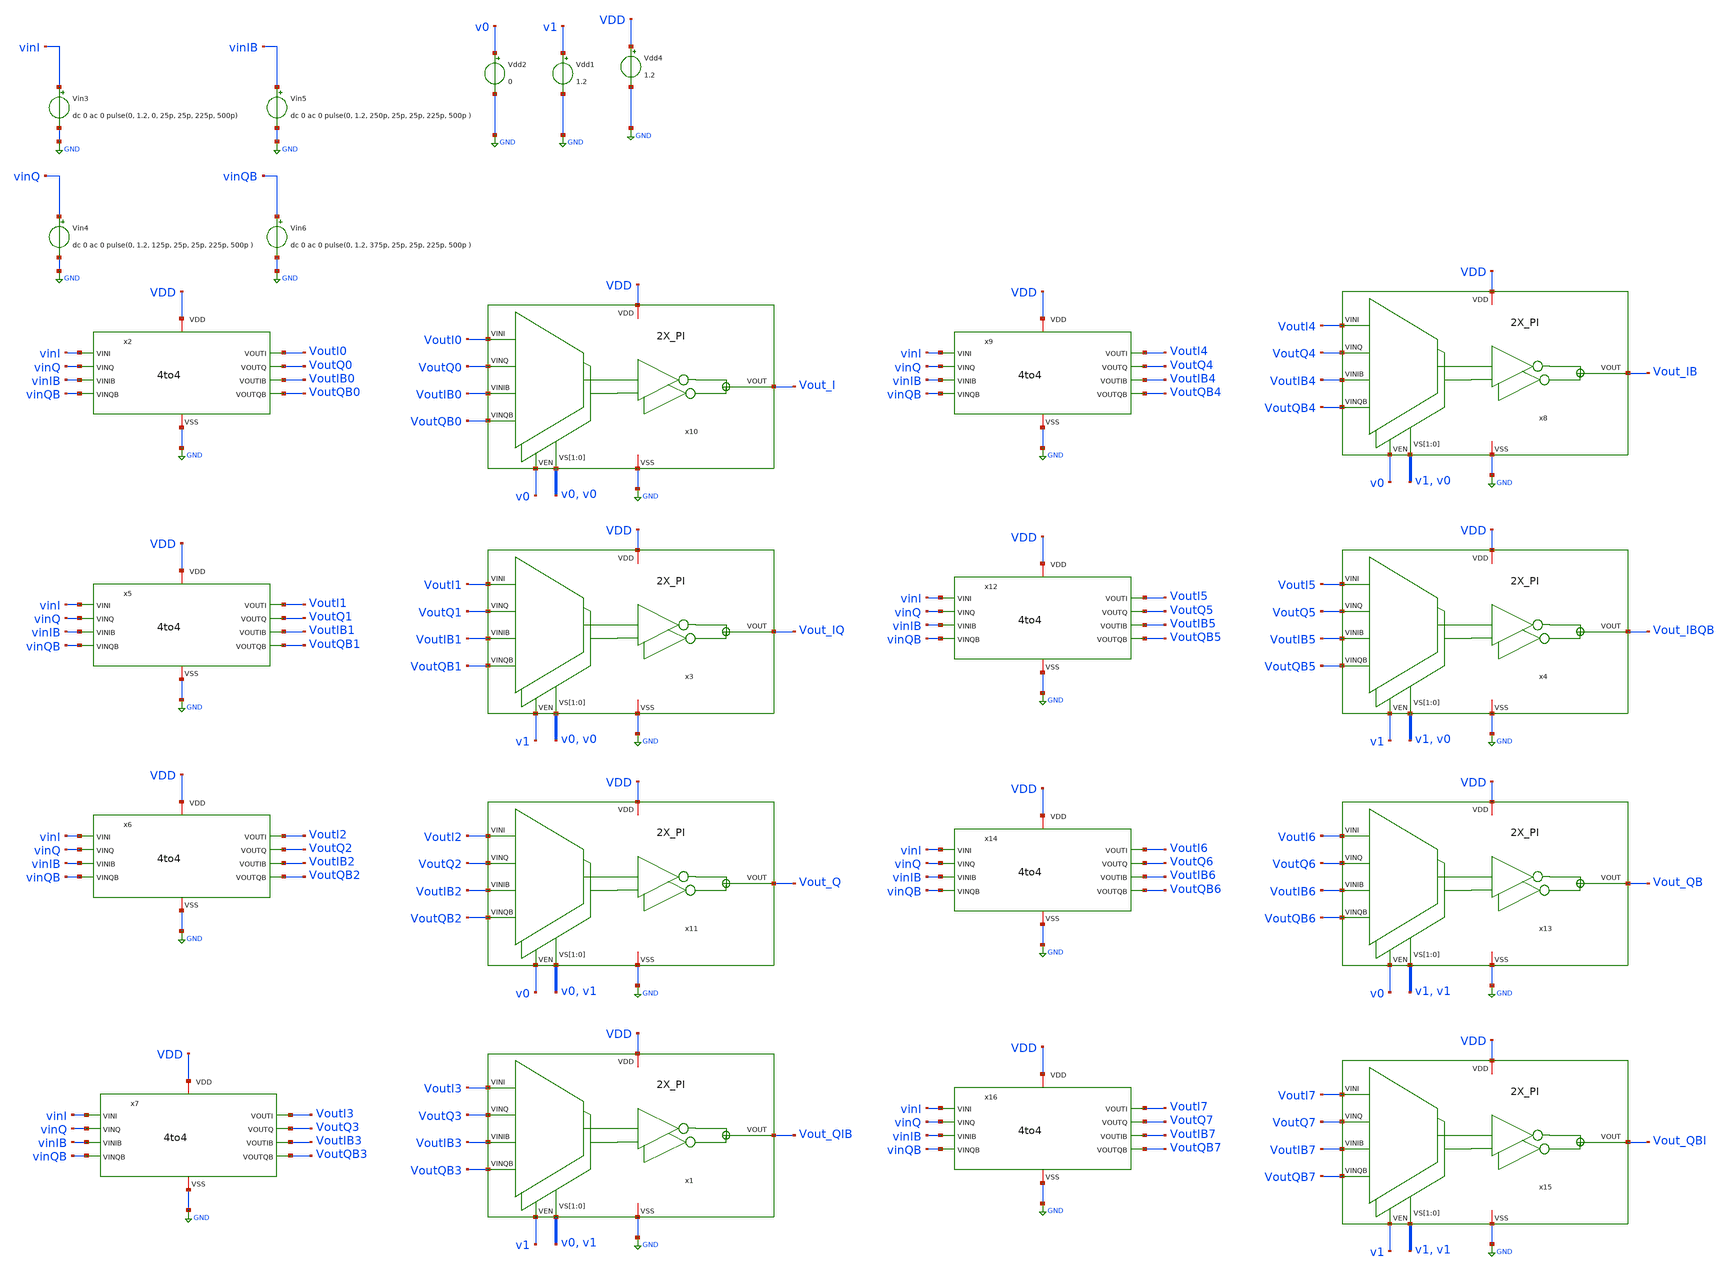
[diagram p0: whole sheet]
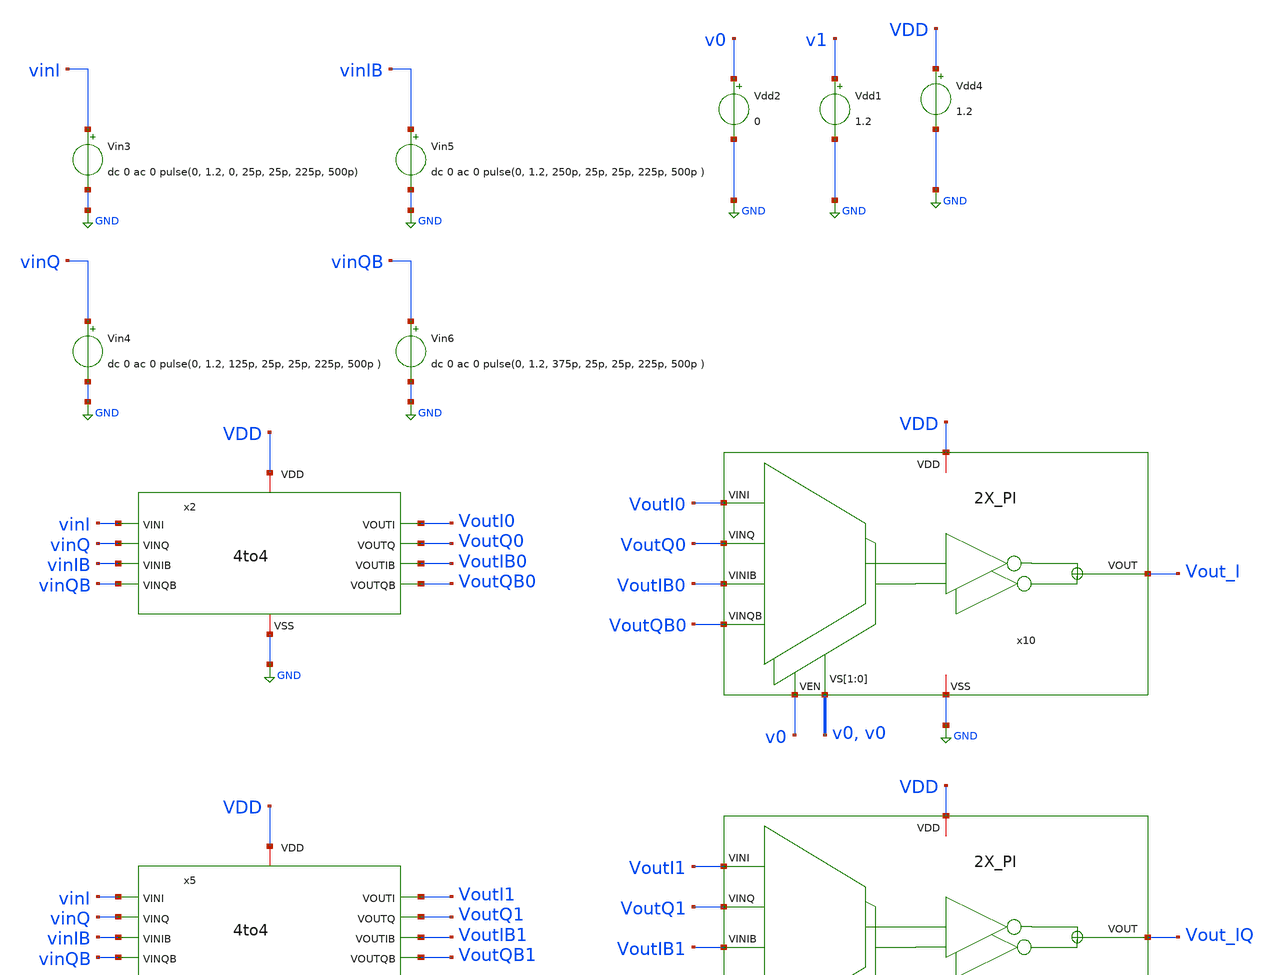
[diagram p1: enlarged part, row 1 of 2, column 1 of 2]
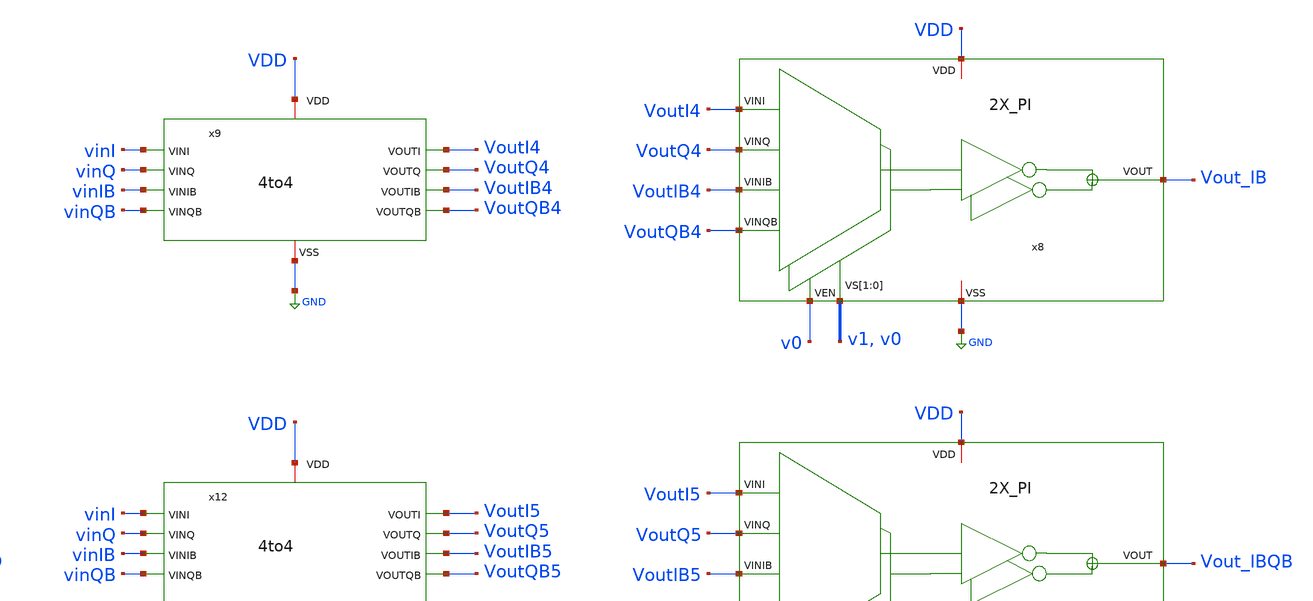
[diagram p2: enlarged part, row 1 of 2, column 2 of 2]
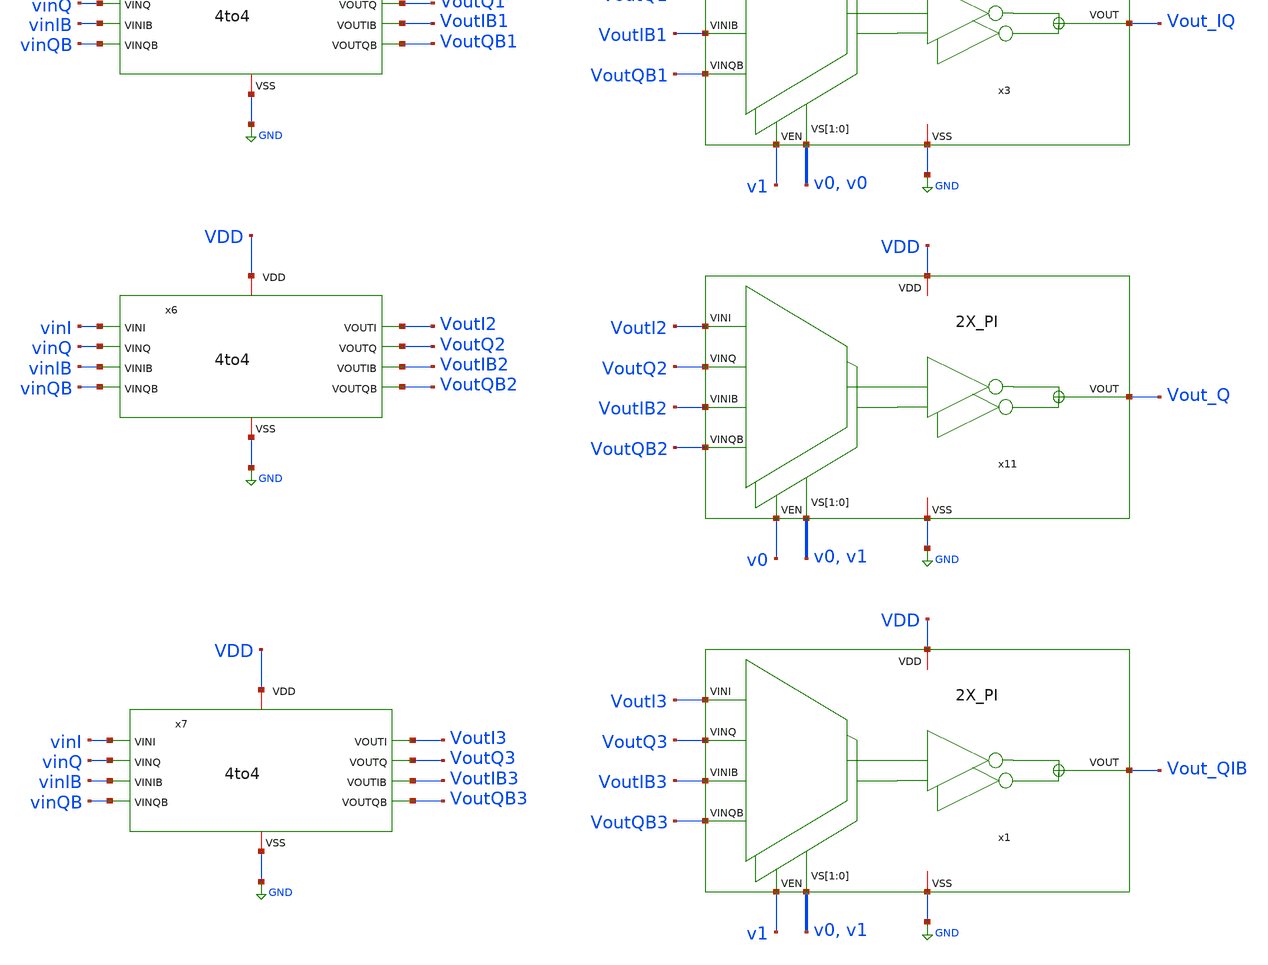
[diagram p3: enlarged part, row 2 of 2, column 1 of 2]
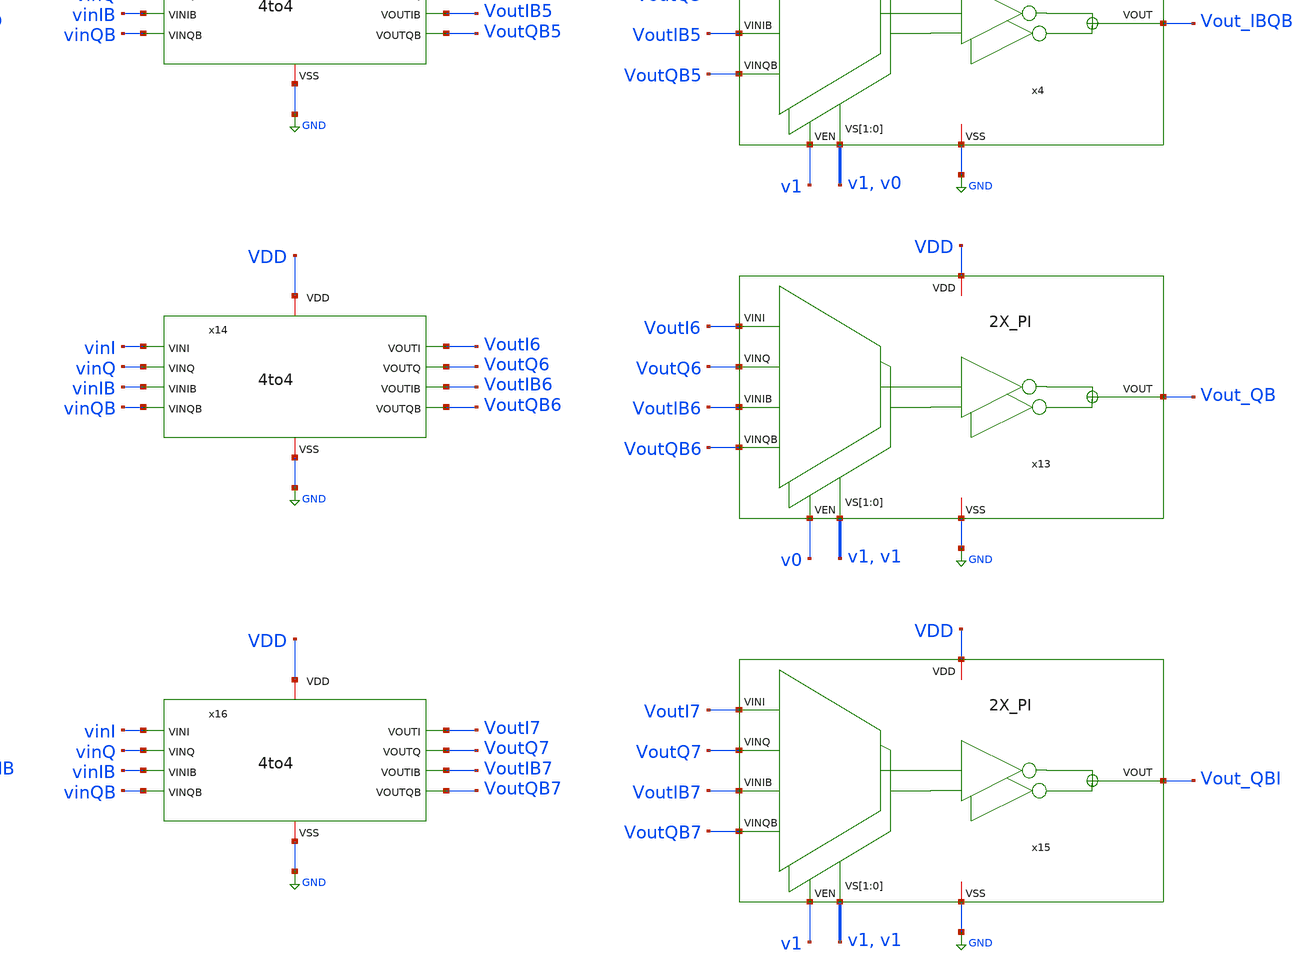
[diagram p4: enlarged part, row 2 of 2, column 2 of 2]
** sch_path: tb_2X_PI_2.sch
**.subckt tb_2X_PI_2
Vdd4 VDD GND 1.2
x1 Vout_QIB v1 VoutI3 VoutQ3 VDD v0 v1 VoutIB3 GND VoutQB3 2X_PI
Vdd1 v1 GND 1.2
Vdd2 v0 GND 0
Vin3 vinI GND dc 0 ac 0 pulse(0, 1.2, 0, 25p, 25p, 225p, 500p)
Vin4 vinQ GND dc 0 ac 0 pulse(0, 1.2, 125p, 25p, 25p, 225p, 500p )
Vin5 vinIB GND dc 0 ac 0 pulse(0, 1.2, 250p, 25p, 25p, 225p, 500p )
Vin6 vinQB GND dc 0 ac 0 pulse(0, 1.2, 375p, 25p, 25p, 225p, 500p )
x2 VDD vinI VoutI0 VoutQ0 vinQ vinIB VoutIB0 vinQB VoutQB0 GND 4to4
x3 Vout_IQ v1 VoutI1 VoutQ1 VDD v0 v0 VoutIB1 GND VoutQB1 2X_PI
x4 Vout_IBQB v1 VoutI5 VoutQ5 VDD v1 v0 VoutIB5 GND VoutQB5 2X_PI
x5 VDD vinI VoutI1 VoutQ1 vinQ vinIB VoutIB1 vinQB VoutQB1 GND 4to4
x6 VDD vinI VoutI2 VoutQ2 vinQ vinIB VoutIB2 vinQB VoutQB2 GND 4to4
x7 VDD vinI VoutI3 VoutQ3 vinQ vinIB VoutIB3 vinQB VoutQB3 GND 4to4
x8 Vout_IB v0 VoutI4 VoutQ4 VDD v1 v0 VoutIB4 GND VoutQB4 2X_PI
x9 VDD vinI VoutI4 VoutQ4 vinQ vinIB VoutIB4 vinQB VoutQB4 GND 4to4
x10 Vout_I v0 VoutI0 VoutQ0 VDD v0 v0 VoutIB0 GND VoutQB0 2X_PI
x11 Vout_Q v0 VoutI2 VoutQ2 VDD v0 v1 VoutIB2 GND VoutQB2 2X_PI
x12 VDD vinI VoutI5 VoutQ5 vinQ vinIB VoutIB5 vinQB VoutQB5 GND 4to4
x13 Vout_QB v0 VoutI6 VoutQ6 VDD v1 v1 VoutIB6 GND VoutQB6 2X_PI
x14 VDD vinI VoutI6 VoutQ6 vinQ vinIB VoutIB6 vinQB VoutQB6 GND 4to4
x15 Vout_QBI v1 VoutI7 VoutQ7 VDD v1 v1 VoutIB7 GND VoutQB7 2X_PI
x16 VDD vinI VoutI7 VoutQ7 vinQ vinIB VoutIB7 vinQB VoutQB7 GND 4to4
**** begin user architecture code


.param temp=27
.control
save all
tran 5p 1.5n

meas tran tPWI TRIG v(Vout_I) VAl=0.6 RISE=1 TARG v(Vout_I) VAl=0.6 FALL=1
meas tran tPWIQ TRIG v(Vout_IQ) VAl=0.6 RISE=1 TARG v(Vout_IQ) VAl=0.6 FALL=1
meas tran tPWQ TRIG v(Vout_Q) VAl=0.6 RISE=1 TARG v(Vout_Q) VAl=0.6 FALL=1
meas tran tPWQIB TRIG v(Vout_QIB) VAl=0.6 RISE=1 TARG v(Vout_QIB) VAl=0.6 FALL=1
meas tran tPWIB TRIG v(Vout_IB) VAl=0.6 RISE=1 TARG v(Vout_IB) VAl=0.6 FALL=1
meas tran tPWIBQB TRIG v(Vout_IBQB) VAl=0.6 RISE=1 TARG v(Vout_IBQB) VAl=0.6 FALL=1
meas tran tPWQB TRIG v(Vout_QB) VAl=0.6 RISE=1 TARG v(Vout_QB) VAl=0.6 FALL=1
meas tran tPWQBI TRIG v(Vout_QBI) VAl=0.6 RISE=1 TARG v(Vout_QBI) VAl=0.6 FALL=1


meas tran tskewI_IQ TRIG v(Vout_I) VAl=0.6 RISE=1 TARG v(Vout_IQ) VAl=0.6 RISE=1
meas tran tskewIQ_Q TRIG v(Vout_IQ) VAl=0.6 RISE=1 TARG v(Vout_Q) VAl=0.6 RISE=1
meas tran tskewQ_QIB TRIG v(Vout_Q) VAl=0.6 RISE=1 TARG v(Vout_QIB) VAl=0.6 RISE=1
meas tran tskewQIB_IB TRIG v(Vout_QIB) VAl=0.6 RISE=1 TARG v(Vout_IB) VAl=0.6 RISE=1
meas tran tskewIB_IBQB TRIG v(Vout_IB) VAl=0.6 RISE=1 TARG v(Vout_IBQB) VAl=0.6 RISE=1
meas tran tskewIBQB_QB TRIG v(Vout_IBQB) VAl=0.6 RISE=1 TARG v(Vout_QB) VAl=0.6 RISE=1
meas tran tskewQB_QBI TRIG v(Vout_QB) VAl=0.6 RISE=1 TARG v(Vout_QBI) VAl=0.6 RISE=1
meas tran tskewQBI_I TRIG v(Vout_QBI) VAl=0.6 RISE=1 TARG v(Vout_I) VAl=0.6 RISE=2


write tran_logic_not.raw
.endc



.lib cornerMOSlv.lib mos_tt

**** end user architecture code
**.ends
.GLOBAL GND
.end
